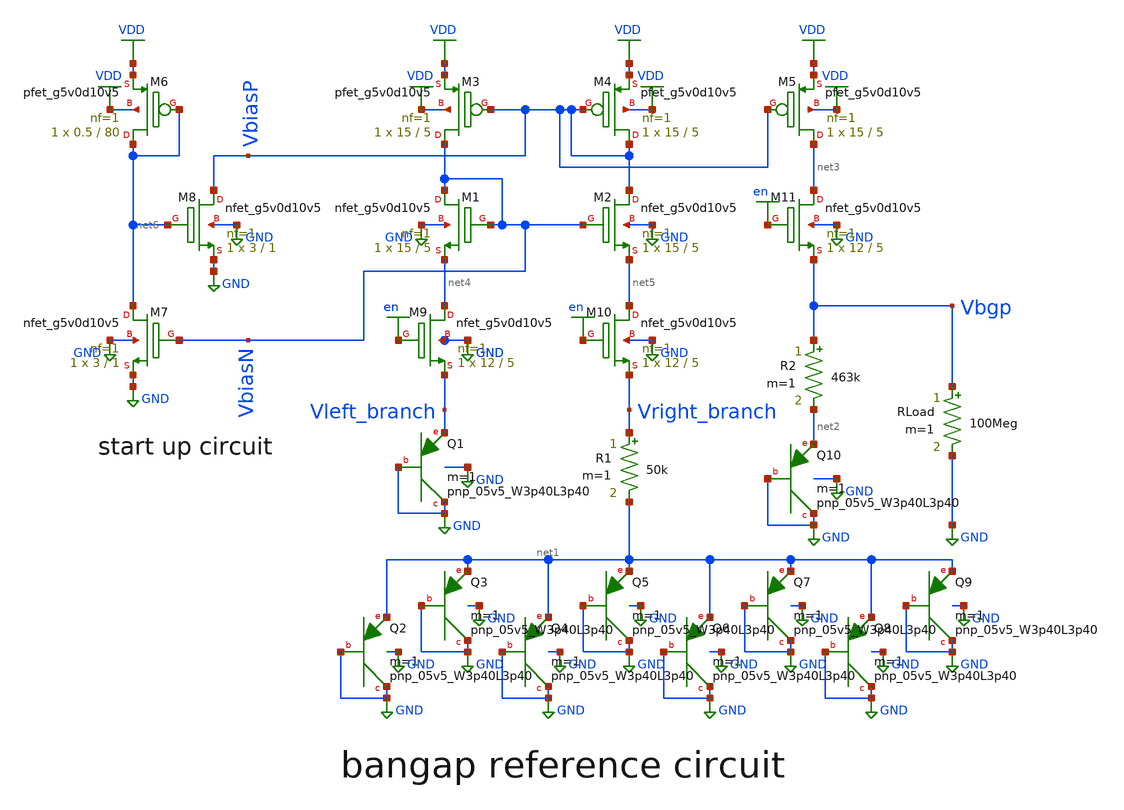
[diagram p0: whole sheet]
** sch_path: pre-layout/attempt_2/spice-deck/bandgap_schematic.sch
**.subckt bandgap_schematic
XM1 VbiasN VbiasN net4 GND sky130_fd_pr__nfet_g5v0d10v5 L=5 W=15 nf=1 ad='int((nf+1)/2) * W/nf * 0.29'
+ as='int((nf+2)/2) * W/nf * 0.29' pd='2*int((nf+1)/2) * (W/nf + 0.29)' ps='2*int((nf+2)/2) * (W/nf + 0.29)'
+ nrd='0.29 / W' nrs='0.29 / W' sa=0 sb=0 sd=0 mult=1 m=1
XM2 VbiasP VbiasN net5 GND sky130_fd_pr__nfet_g5v0d10v5 L=5 W=15 nf=1 ad='int((nf+1)/2) * W/nf * 0.29'
+ as='int((nf+2)/2) * W/nf * 0.29' pd='2*int((nf+1)/2) * (W/nf + 0.29)' ps='2*int((nf+2)/2) * (W/nf + 0.29)'
+ nrd='0.29 / W' nrs='0.29 / W' sa=0 sb=0 sd=0 mult=1 m=1
XM3 VbiasN VbiasP VDD VDD sky130_fd_pr__pfet_g5v0d10v5 L=5 W=15 nf=1 ad='int((nf+1)/2) * W/nf * 0.29'
+ as='int((nf+2)/2) * W/nf * 0.29' pd='2*int((nf+1)/2) * (W/nf + 0.29)' ps='2*int((nf+2)/2) * (W/nf + 0.29)'
+ nrd='0.29 / W' nrs='0.29 / W' sa=0 sb=0 sd=0 mult=1 m=1
XQ1 GND GND Vleft_branch sky130_fd_pr__pnp_05v5_W3p40L3p40 m=1
XQ2 GND GND net1 sky130_fd_pr__pnp_05v5_W3p40L3p40 m=1
XM5 net3 VbiasP VDD VDD sky130_fd_pr__pfet_g5v0d10v5 L=5 W=15 nf=1 ad='int((nf+1)/2) * W/nf * 0.29' as='int((nf+2)/2) * W/nf * 0.29'
+ pd='2*int((nf+1)/2) * (W/nf + 0.29)' ps='2*int((nf+2)/2) * (W/nf + 0.29)' nrd='0.29 / W' nrs='0.29 / W'
+ sa=0 sb=0 sd=0 mult=1 m=1
XQ3 GND GND net1 sky130_fd_pr__pnp_05v5_W3p40L3p40 m=1
XQ4 GND GND net1 sky130_fd_pr__pnp_05v5_W3p40L3p40 m=1
XQ5 GND GND net1 sky130_fd_pr__pnp_05v5_W3p40L3p40 m=1
XQ6 GND GND net1 sky130_fd_pr__pnp_05v5_W3p40L3p40 m=1
XQ7 GND GND net1 sky130_fd_pr__pnp_05v5_W3p40L3p40 m=1
XQ8 GND GND net1 sky130_fd_pr__pnp_05v5_W3p40L3p40 m=1
XQ9 GND GND net1 sky130_fd_pr__pnp_05v5_W3p40L3p40 m=1
R1 Vright_branch net1 50k m=1
R2 Vbgp net2 463k m=1
XQ10 GND GND net2 sky130_fd_pr__pnp_05v5_W3p40L3p40 m=1
XM4 VbiasP VbiasP VDD VDD sky130_fd_pr__pfet_g5v0d10v5 L=5 W=15 nf=1 ad='int((nf+1)/2) * W/nf * 0.29'
+ as='int((nf+2)/2) * W/nf * 0.29' pd='2*int((nf+1)/2) * (W/nf + 0.29)' ps='2*int((nf+2)/2) * (W/nf + 0.29)'
+ nrd='0.29 / W' nrs='0.29 / W' sa=0 sb=0 sd=0 mult=1 m=1
XM7 net6 VbiasN GND GND sky130_fd_pr__nfet_g5v0d10v5 L=1 W=3 nf=1 ad='int((nf+1)/2) * W/nf * 0.29' as='int((nf+2)/2) * W/nf * 0.29'
+ pd='2*int((nf+1)/2) * (W/nf + 0.29)' ps='2*int((nf+2)/2) * (W/nf + 0.29)' nrd='0.29 / W' nrs='0.29 / W'
+ sa=0 sb=0 sd=0 mult=1 m=1
XM8 VbiasP net6 GND GND sky130_fd_pr__nfet_g5v0d10v5 L=1 W=3 nf=1 ad='int((nf+1)/2) * W/nf * 0.29' as='int((nf+2)/2) * W/nf * 0.29'
+ pd='2*int((nf+1)/2) * (W/nf + 0.29)' ps='2*int((nf+2)/2) * (W/nf + 0.29)' nrd='0.29 / W' nrs='0.29 / W'
+ sa=0 sb=0 sd=0 mult=1 m=1
RLoad Vbgp GND 100Meg m=1
XM9 net4 en Vleft_branch GND sky130_fd_pr__nfet_g5v0d10v5 L=5 W=12 nf=1 ad='int((nf+1)/2) * W/nf * 0.29'
+ as='int((nf+2)/2) * W/nf * 0.29' pd='2*int((nf+1)/2) * (W/nf + 0.29)' ps='2*int((nf+2)/2) * (W/nf + 0.29)'
+ nrd='0.29 / W' nrs='0.29 / W' sa=0 sb=0 sd=0 mult=1 m=1
XM10 net5 en Vright_branch GND sky130_fd_pr__nfet_g5v0d10v5 L=5 W=12 nf=1 ad='int((nf+1)/2) * W/nf * 0.29'
+ as='int((nf+2)/2) * W/nf * 0.29' pd='2*int((nf+1)/2) * (W/nf + 0.29)' ps='2*int((nf+2)/2) * (W/nf + 0.29)'
+ nrd='0.29 / W' nrs='0.29 / W' sa=0 sb=0 sd=0 mult=1 m=1
XM11 net3 en Vbgp GND sky130_fd_pr__nfet_g5v0d10v5 L=5 W=12 nf=1 ad='int((nf+1)/2) * W/nf * 0.29' as='int((nf+2)/2) * W/nf * 0.29'
+ pd='2*int((nf+1)/2) * (W/nf + 0.29)' ps='2*int((nf+2)/2) * (W/nf + 0.29)' nrd='0.29 / W' nrs='0.29 / W'
+ sa=0 sb=0 sd=0 mult=1 m=1
XM6 net6 net6 VDD VDD sky130_fd_pr__pfet_g5v0d10v5 L=80 W=0.5 nf=1 ad='int((nf+1)/2) * W/nf * 0.29' as='int((nf+2)/2) * W/nf * 0.29'
+ pd='2*int((nf+1)/2) * (W/nf + 0.29)' ps='2*int((nf+2)/2) * (W/nf + 0.29)' nrd='0.29 / W' nrs='0.29 / W'
+ sa=0 sb=0 sd=0 mult=1 m=1
**** begin user architecture code


.lib /home/swarup/Desktop/vsdflow/work/tools/openlane_working_dir/pdks/skywater-pdk/libraries/sky130_fd_pr_ngspice/latest/models/sky130.lib.spice tt
.include /home/swarup/Desktop/vsdflow/work/tools/openlane_working_dir/pdks/skywater-pdk/libraries/sky130_fd_pr_ngspice/latest/models/sky130_fd_pr__model__pnp.model.spice
.options savecurrents

*** plot vbgp with variation in supply voltage
*Vdd VDD GND 3.3
*V_en en GND 3.3
*.dc Vdd 2 4 0.1
*.control
*run
*print Vbgp
*plot V(Vbgp)
*.endc

*** plot vbgp with variation in temperature @3.3V
*Vdd VDD GND 3.3
*V_en en GND 3.3
*.dc temp -40 140 1
*.control
*run
*print V(Vbgp)
*plot V(Vbgp)
*.endc

*** plot voltage coefficient
*Vdd VDD GND 3.3
*V_en en GND 3.3
*.dc Vdd 2 4 0.1
*.control
*run
*plot deriv(V(Vbgp))
*.endc

*** plot temperature coefficient
*Vdd VDD GND 3.3
*V_en en GND 3.3
*.dc temp -40 140 1
*.control
*run
*plot deriv(V(Vbgp))/1.202344
*.endc

*** check start up circuit
V_en en GND 3.3
Vdd VDD GND PULSE(0 3.3 50us 40us 0us 200us 400us 0)
.tran 1us 200us
.control
run
plot V(Vdd) V(Vbgp)
.endc

*** enable pin
*Vdd VDD GND 3.3
*V_en en GND PULSE(0 3.3 50us 0 0 10us 20us 0)
*.tran 1u 150us
*.control
*run
*plot V(en) V(Vbgp)
*.endc


**** end user architecture code
**.ends
.GLOBAL GND
.GLOBAL VDD
.GLOBAL en
.end
